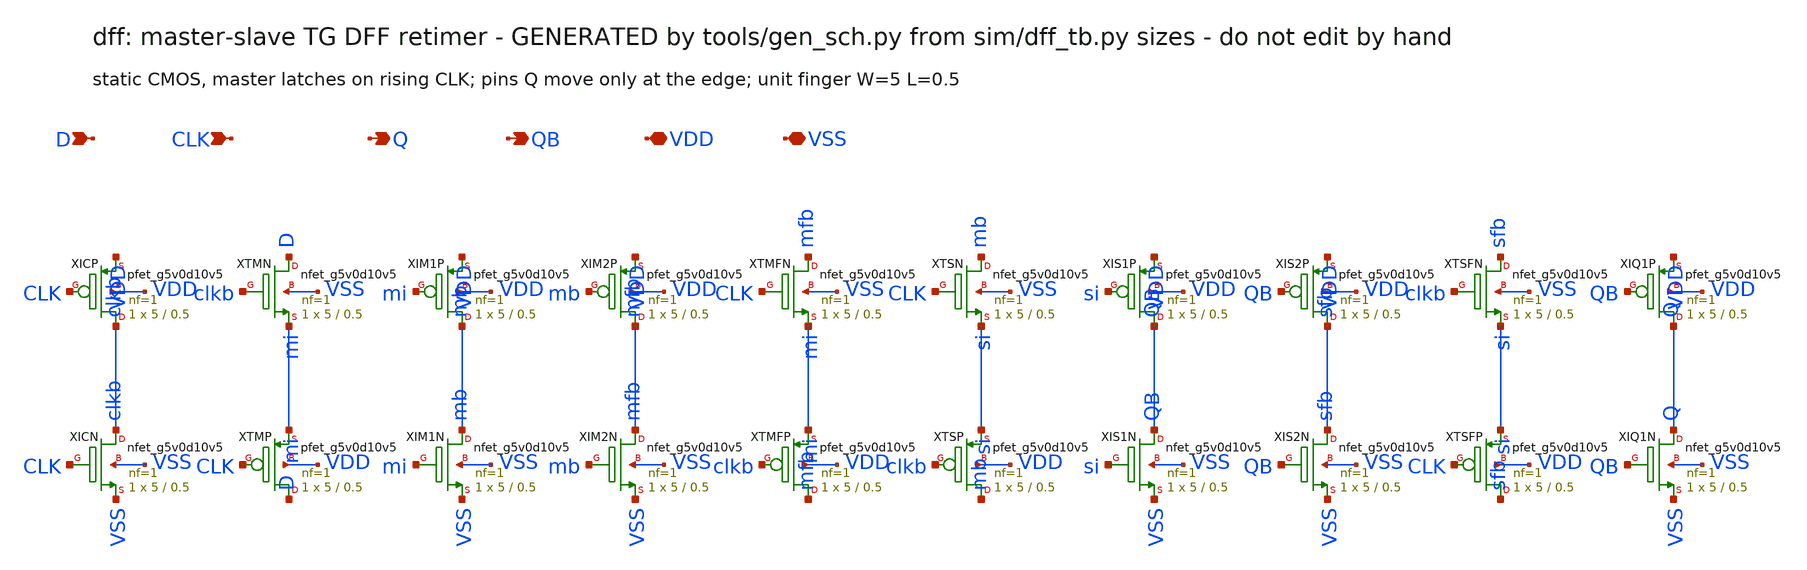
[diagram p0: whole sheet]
** sch_path: xschem/dff.sch
**.subckt dff D CLK Q QB VDD VSS
*.ipin D
*.ipin CLK
*.opin Q
*.opin QB
*.iopin VDD
*.iopin VSS
XXICP clkb CLK VDD VDD sky130_fd_pr__pfet_g5v0d10v5 L=0.5 W=5 nf=1 ad=0 as=0 pd=0 ps=0 nrd=0 nrs=0
+ sa=0 sb=0 sd=0 mult=1 m=1
XXICN clkb CLK VSS VSS sky130_fd_pr__nfet_g5v0d10v5 L=0.5 W=5 nf=1 ad=0 as=0 pd=0 ps=0 nrd=0 nrs=0
+ sa=0 sb=0 sd=0 mult=1 m=1
XXTMN D clkb mi VSS sky130_fd_pr__nfet_g5v0d10v5 L=0.5 W=5 nf=1 ad=0 as=0 pd=0 ps=0 nrd=0 nrs=0 sa=0
+ sb=0 sd=0 mult=1 m=1
XXTMP D CLK mi VDD sky130_fd_pr__pfet_g5v0d10v5 L=0.5 W=5 nf=1 ad=0 as=0 pd=0 ps=0 nrd=0 nrs=0 sa=0
+ sb=0 sd=0 mult=1 m=1
XXIM1P mb mi VDD VDD sky130_fd_pr__pfet_g5v0d10v5 L=0.5 W=5 nf=1 ad=0 as=0 pd=0 ps=0 nrd=0 nrs=0
+ sa=0 sb=0 sd=0 mult=1 m=1
XXIM1N mb mi VSS VSS sky130_fd_pr__nfet_g5v0d10v5 L=0.5 W=5 nf=1 ad=0 as=0 pd=0 ps=0 nrd=0 nrs=0
+ sa=0 sb=0 sd=0 mult=1 m=1
XXIM2P mfb mb VDD VDD sky130_fd_pr__pfet_g5v0d10v5 L=0.5 W=5 nf=1 ad=0 as=0 pd=0 ps=0 nrd=0 nrs=0
+ sa=0 sb=0 sd=0 mult=1 m=1
XXIM2N mfb mb VSS VSS sky130_fd_pr__nfet_g5v0d10v5 L=0.5 W=5 nf=1 ad=0 as=0 pd=0 ps=0 nrd=0 nrs=0
+ sa=0 sb=0 sd=0 mult=1 m=1
XXTMFN mfb CLK mi VSS sky130_fd_pr__nfet_g5v0d10v5 L=0.5 W=5 nf=1 ad=0 as=0 pd=0 ps=0 nrd=0 nrs=0
+ sa=0 sb=0 sd=0 mult=1 m=1
XXTMFP mfb clkb mi VDD sky130_fd_pr__pfet_g5v0d10v5 L=0.5 W=5 nf=1 ad=0 as=0 pd=0 ps=0 nrd=0 nrs=0
+ sa=0 sb=0 sd=0 mult=1 m=1
XXTSN mb CLK si VSS sky130_fd_pr__nfet_g5v0d10v5 L=0.5 W=5 nf=1 ad=0 as=0 pd=0 ps=0 nrd=0 nrs=0 sa=0
+ sb=0 sd=0 mult=1 m=1
XXTSP mb clkb si VDD sky130_fd_pr__pfet_g5v0d10v5 L=0.5 W=5 nf=1 ad=0 as=0 pd=0 ps=0 nrd=0 nrs=0
+ sa=0 sb=0 sd=0 mult=1 m=1
XXIS1P QB si VDD VDD sky130_fd_pr__pfet_g5v0d10v5 L=0.5 W=5 nf=1 ad=0 as=0 pd=0 ps=0 nrd=0 nrs=0
+ sa=0 sb=0 sd=0 mult=1 m=1
XXIS1N QB si VSS VSS sky130_fd_pr__nfet_g5v0d10v5 L=0.5 W=5 nf=1 ad=0 as=0 pd=0 ps=0 nrd=0 nrs=0
+ sa=0 sb=0 sd=0 mult=1 m=1
XXIS2P sfb QB VDD VDD sky130_fd_pr__pfet_g5v0d10v5 L=0.5 W=5 nf=1 ad=0 as=0 pd=0 ps=0 nrd=0 nrs=0
+ sa=0 sb=0 sd=0 mult=1 m=1
XXIS2N sfb QB VSS VSS sky130_fd_pr__nfet_g5v0d10v5 L=0.5 W=5 nf=1 ad=0 as=0 pd=0 ps=0 nrd=0 nrs=0
+ sa=0 sb=0 sd=0 mult=1 m=1
XXTSFN sfb clkb si VSS sky130_fd_pr__nfet_g5v0d10v5 L=0.5 W=5 nf=1 ad=0 as=0 pd=0 ps=0 nrd=0 nrs=0
+ sa=0 sb=0 sd=0 mult=1 m=1
XXTSFP sfb CLK si VDD sky130_fd_pr__pfet_g5v0d10v5 L=0.5 W=5 nf=1 ad=0 as=0 pd=0 ps=0 nrd=0 nrs=0
+ sa=0 sb=0 sd=0 mult=1 m=1
XXIQ1P Q QB VDD VDD sky130_fd_pr__pfet_g5v0d10v5 L=0.5 W=5 nf=1 ad=0 as=0 pd=0 ps=0 nrd=0 nrs=0 sa=0
+ sb=0 sd=0 mult=1 m=1
XXIQ1N Q QB VSS VSS sky130_fd_pr__nfet_g5v0d10v5 L=0.5 W=5 nf=1 ad=0 as=0 pd=0 ps=0 nrd=0 nrs=0 sa=0
+ sb=0 sd=0 mult=1 m=1
**.ends
.end
